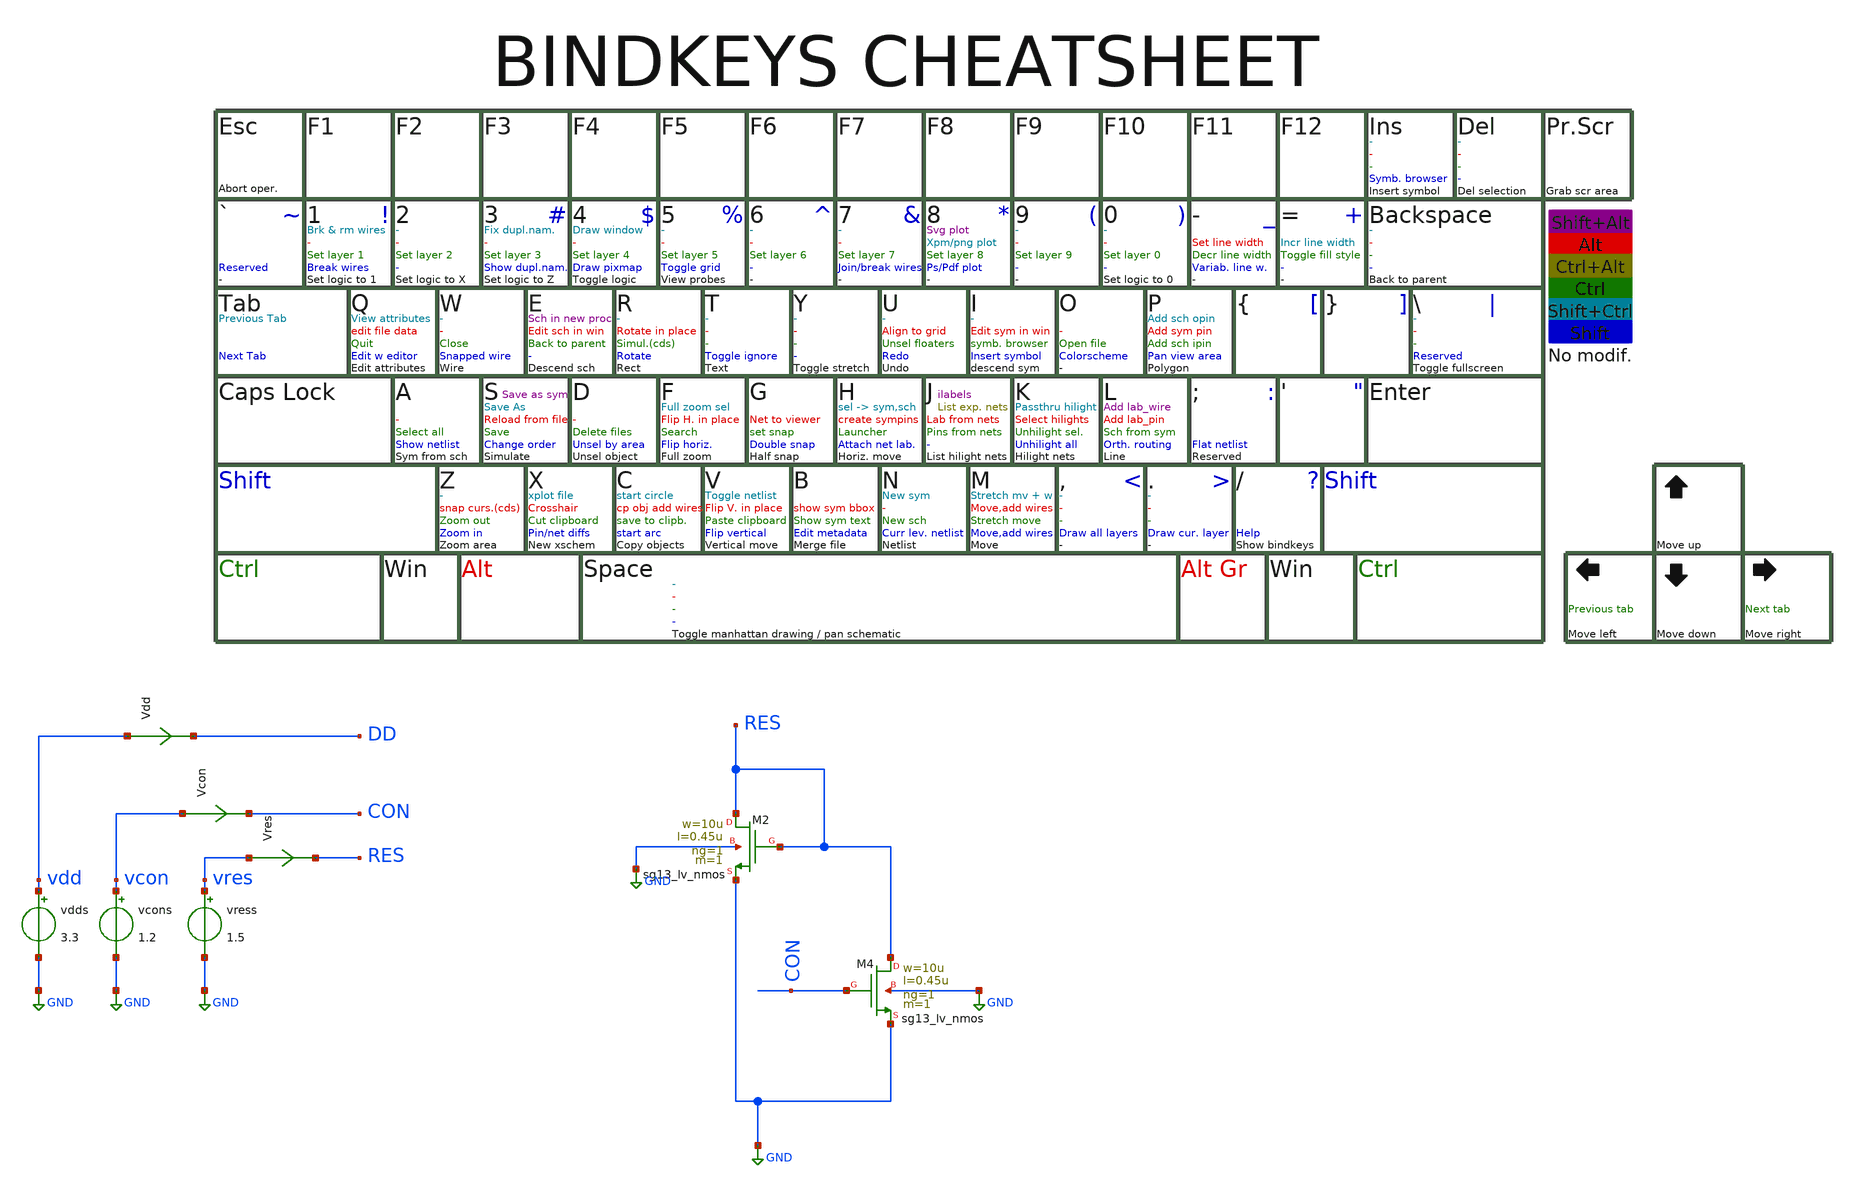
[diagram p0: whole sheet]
** sch_path: macros/heichips26_analog_project/macros/floating-gate/testbenches/xschem/plm.sch
**.subckt plm
Vres vres RES 0
.save i(vres)
vress vres GND 1.5
vcons vcon GND 1.2
vdds vdd GND 3.3
Vcon vcon CON 0
.save i(vcon)
Vdd vdd DD 0
.save i(vdd)
XM2 RES RES GND GND sg13_lv_nmos w=10u l=0.45u ng=1 m=1 mm_ok=1
XM4 RES CON GND GND sg13_lv_nmos w=10u l=0.45u ng=1 m=1 mm_ok=1
**** begin user architecture code


* .include ../../../netlist/pex/inverter_magic_pex_3.spice
.param temp=27
.options savecurrents klu method=gear reltol=1e-3 abstol=1e-15 gmin=1e-15
.control
save all
set appendwrite

* DC Sweep
* dc vcon 0.001 2 1m
* remzerovec

* plot v(vres)/i(Vres)
*plot v(VStage1)
*plot v(VStage2)



let vcc = 0.1
repeat 5
  alter vres $&vcc

  * DC Sweep
  * dc VS -1.5 1.5 1m
  dc vcon 0.001 1.5 1m
  remzerovec
  let vcc = vcc + 0.2
end
set appendwrite

* Plotting
plot dc1.v(vres)/(dc1.i(Vres)) dc2.v(vres)/(dc2.i(Vres)) dc3.v(vres)/(dc3.i(Vres))
+ dc4.v(vres)/(dc4.i(Vres)) dc5.v(vres)/(dc5.i(Vres))
* Write Data
unset appendwrite
set wr_vecnames
set wr_singlescale

*quit
.endc



.lib cornerMOSlv.lib mos_tt
.lib cornerMOShv.lib mos_tt
.lib cornerRES.lib res_typ
.lib cornerDIO.lib dio_tt

**** end user architecture code
**.ends
.GLOBAL GND
.end
